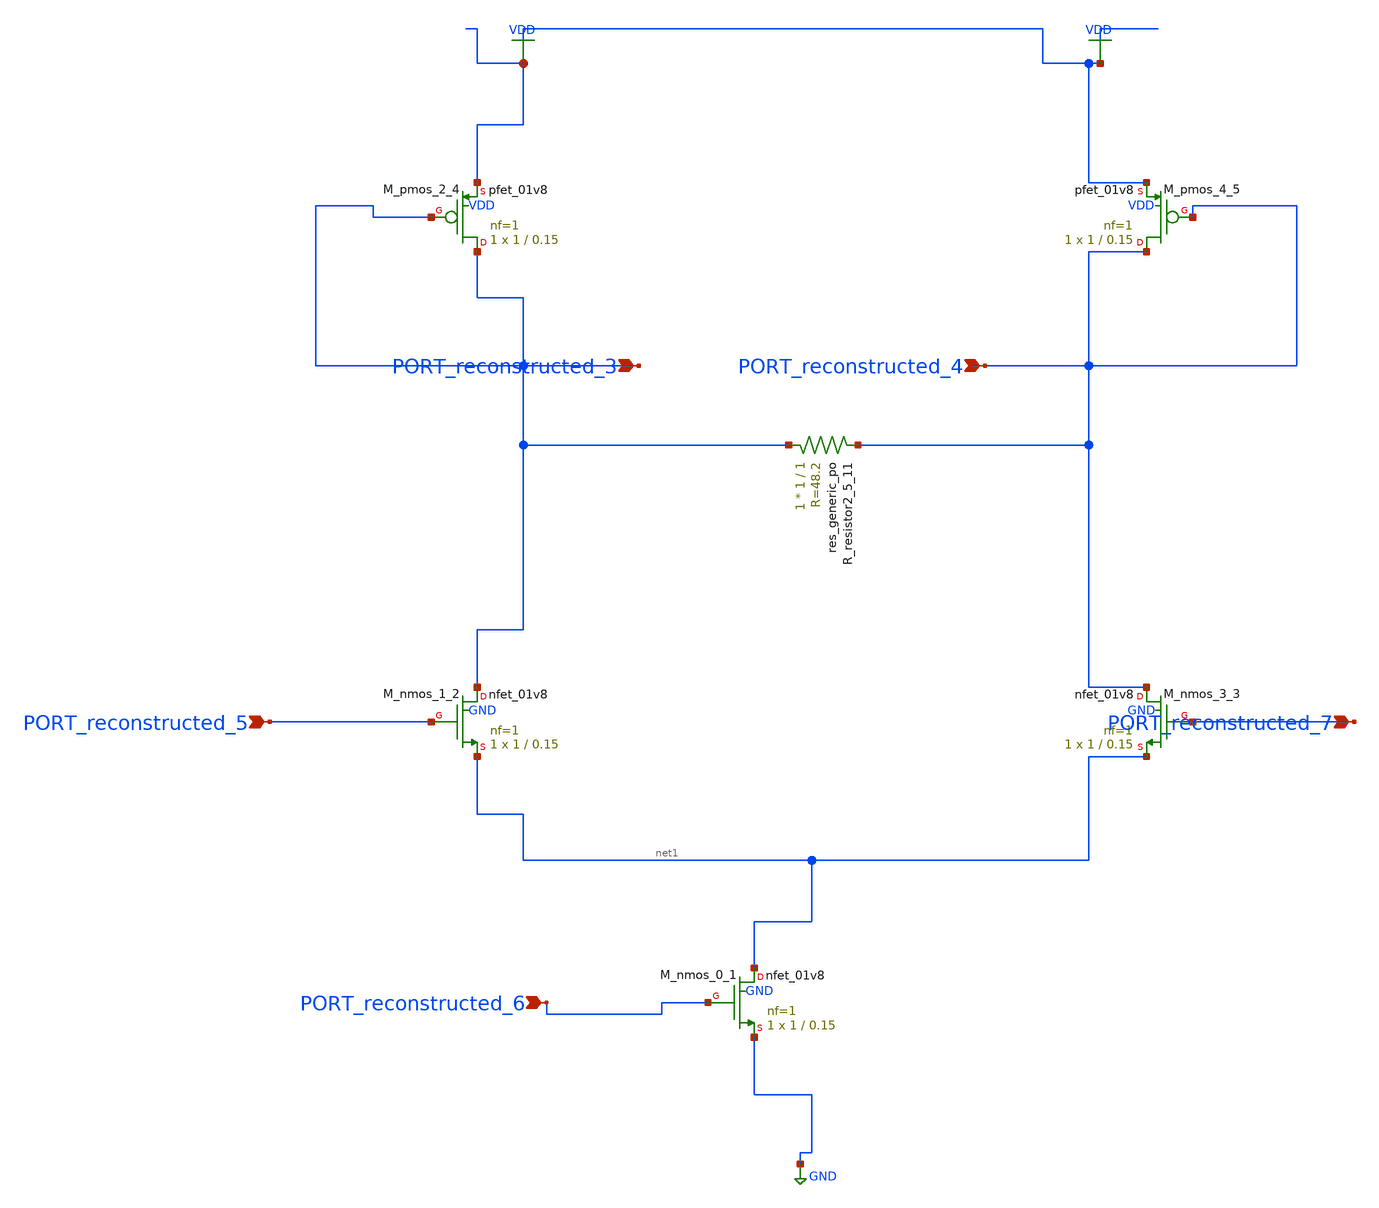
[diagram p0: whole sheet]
** sch_path: schematics/AMSNet/237.sch
**.subckt 237 PORT_reconstructed_5 PORT_reconstructed_4 PORT_reconstructed_3 PORT_reconstructed_6
*+ PORT_reconstructed_7
*.ipin PORT_reconstructed_5
*.ipin PORT_reconstructed_4
*.ipin PORT_reconstructed_3
*.ipin PORT_reconstructed_6
*.ipin PORT_reconstructed_7
XM_nmos_0_1 net1 PORT_reconstructed_6 GND GND sky130_fd_pr__nfet_01v8 L=0.15 W=1 nf=1 ad='int((1 + 1)/2) * 1 / 1 * 0.29'
+ as='int((1 + 2)/2) * 1 / 1 * 0.29' pd='2*int((1 + 1)/2) * (1 / 1 + 0.29)' ps='2*int((1 + 2)/2) * (1 / 1 + 0.29)'
+ nrd='0.29 / 1 ' nrs='0.29 / 1 ' sa=0 sb=0 sd=0 mult=1 m=1
XM_nmos_1_2 PORT_reconstructed_3 PORT_reconstructed_5 net1 GND sky130_fd_pr__nfet_01v8 L=0.15 W=1 nf=1
+ ad='int((1 + 1)/2) * 1 / 1 * 0.29' as='int((1 + 2)/2) * 1 / 1 * 0.29' pd='2*int((1 + 1)/2) * (1 / 1 + 0.29)'
+ ps='2*int((1 + 2)/2) * (1 / 1 + 0.29)' nrd='0.29 / 1 ' nrs='0.29 / 1 ' sa=0 sb=0 sd=0 mult=1 m=1
XM_nmos_3_3 PORT_reconstructed_4 PORT_reconstructed_7 net1 GND sky130_fd_pr__nfet_01v8 L=0.15 W=1 nf=1
+ ad='int((1 + 1)/2) * 1 / 1 * 0.29' as='int((1 + 2)/2) * 1 / 1 * 0.29' pd='2*int((1 + 1)/2) * (1 / 1 + 0.29)'
+ ps='2*int((1 + 2)/2) * (1 / 1 + 0.29)' nrd='0.29 / 1 ' nrs='0.29 / 1 ' sa=0 sb=0 sd=0 mult=1 m=1
XM_pmos_2_4 PORT_reconstructed_3 PORT_reconstructed_3 VDD VDD sky130_fd_pr__pfet_01v8 L=0.15 W=1 nf=1
+ ad='int((1 + 1)/2) * 1 / 1 * 0.29' as='int((1 + 2)/2) * 1 / 1 * 0.29' pd='2*int((1 + 1)/2) * (1 / 1 + 0.29)'
+ ps='2*int((1 + 2)/2) * (1 / 1 + 0.29)' nrd='0.29 / 1 ' nrs='0.29 / 1 ' sa=0 sb=0 sd=0 mult=1 m=1
XM_pmos_4_5 PORT_reconstructed_4 PORT_reconstructed_4 VDD VDD sky130_fd_pr__pfet_01v8 L=0.15 W=1 nf=1
+ ad='int((1 + 1)/2) * 1 / 1 * 0.29' as='int((1 + 2)/2) * 1 / 1 * 0.29' pd='2*int((1 + 1)/2) * (1 / 1 + 0.29)'
+ ps='2*int((1 + 2)/2) * (1 / 1 + 0.29)' nrd='0.29 / 1 ' nrs='0.29 / 1 ' sa=0 sb=0 sd=0 mult=1 m=1
XR_resistor2_5_11 PORT_reconstructed_3 PORT_reconstructed_4 sky130_fd_pr__res_generic_po W=1 L=1 m=1
**.ends
.GLOBAL GND
.GLOBAL VDD
.end
